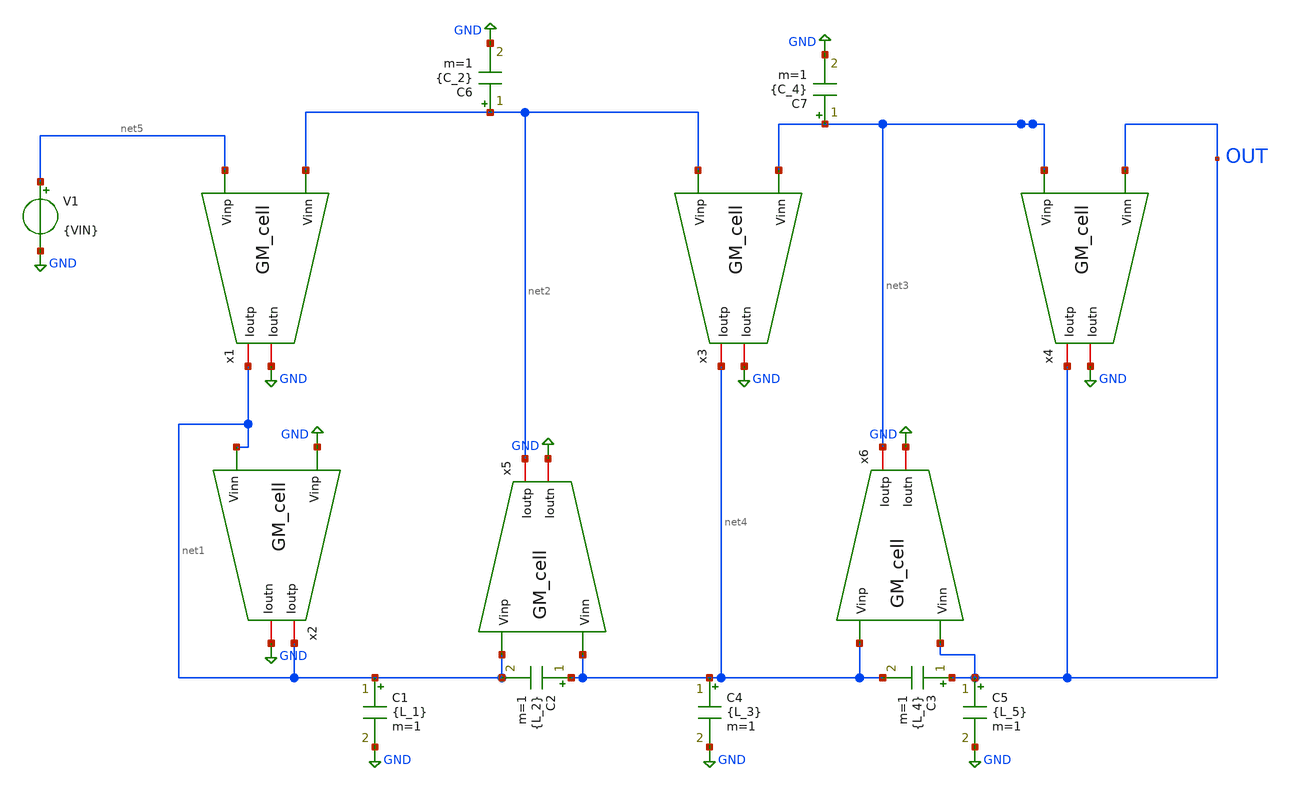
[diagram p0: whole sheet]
** sch_path: LPF design/SCLICAP_TEST/GM_C_filter.sch
**.subckt GM_C_filter
x1 net1 net5 net2 GND GM_cell gm=100u AV=50
x2 net1 GND net1 GND GM_cell gm=100u AV=50
x3 net4 net2 net3 GND GM_cell gm=100u AV=50
x4 OUT net3 OUT GND GM_cell gm=100u AV=50
x5 net2 net1 net4 GND GM_cell gm=100u AV=50
x6 net3 net4 OUT GND GM_cell gm=100u AV=50
C1 net1 GND {L_1} m=1
C2 net4 net1 {L_2} m=1
C3 OUT net4 {L_4} m=1
C4 net4 GND {L_3} m=1
C5 OUT GND {L_5} m=1
C6 net2 GND {C_2} m=1
C7 net3 GND {C_4} m=1
V1 net5 GND {VIN}
**.ends

* expanding   symbol:  GM_cell.sym # of pins=4
** sym_path: LPF design/SCLICAP_TEST/GM_cell.sym
** sch_path: LPF design/SCLICAP_TEST/GM_cell.sch
.subckt GM_cell Ioutp Vinp Vinn Ioutn  gm=100u AV=50
*.ipin Vinp
*.ipin Vinn
*.iopin Ioutn
*.iopin Ioutp
G1 Ioutn Ioutp Vinp Vinn {gm}
R1 Ioutn Ioutp {AV/gm} m=1
.ends

.GLOBAL GND
.end
